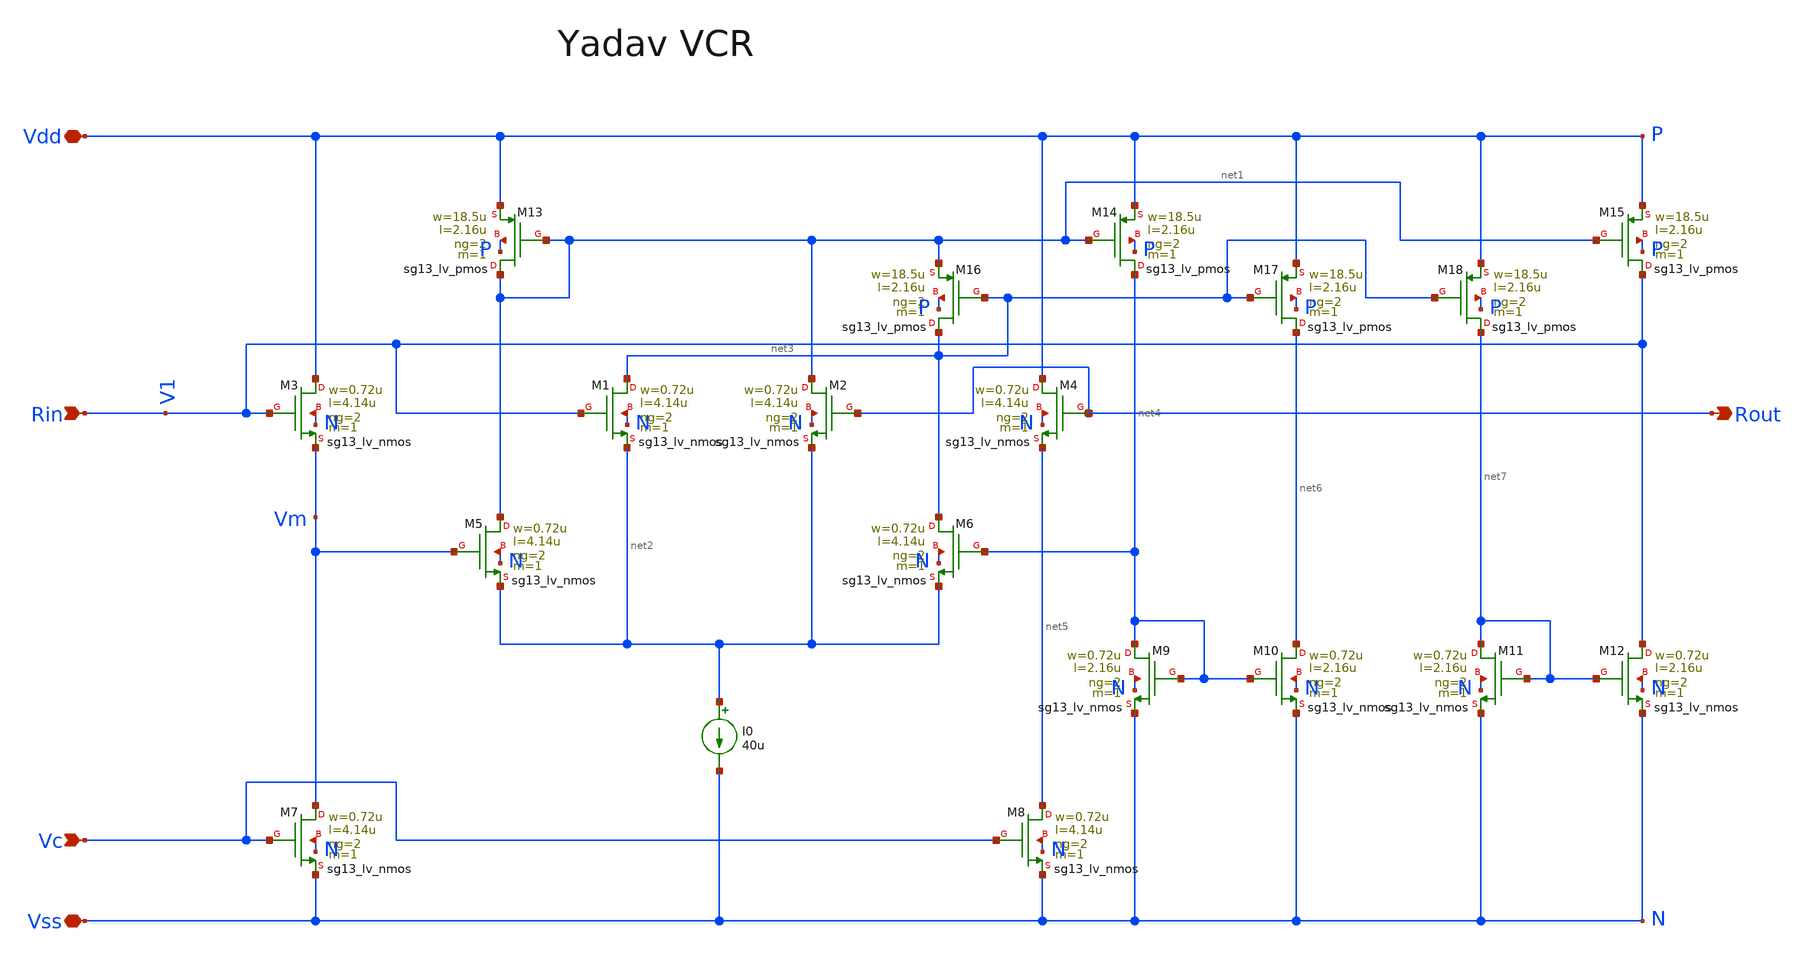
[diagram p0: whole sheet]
** sch_path: macros/heichips26_analog_project/macros/yadav/schematic/xschem/yadav.sch
**.subckt yadav Rin Vc Vss Vdd Rout
*.ipin Rin
*.ipin Vc
*.iopin Vss
*.iopin Vdd
*.opin Rout
XM3 Vdd Rin Vm N sg13_lv_nmos w=0.72u l=4.14u ng=2 m=1 mm_ok=1
XM13 net1 net1 Vdd P sg13_lv_pmos w=18.5u l=2.16u ng=2 m=1 mm_ok=1
XM1 net3 Rin net2 N sg13_lv_nmos w=0.72u l=4.14u ng=2 m=1 mm_ok=1
XM5 net1 Vm net2 N sg13_lv_nmos w=0.72u l=4.14u ng=2 m=1 mm_ok=1
XM2 net1 Rout net2 N sg13_lv_nmos w=0.72u l=4.14u ng=2 m=1 mm_ok=1
XM16 net3 net3 net1 P sg13_lv_pmos w=18.5u l=2.16u ng=2 m=1 mm_ok=1
XM7 Vm Vc Vss N sg13_lv_nmos w=0.72u l=4.14u ng=2 m=1 mm_ok=1
XM6 net3 net4 net2 N sg13_lv_nmos w=0.72u l=4.14u ng=2 m=1 mm_ok=1
XM14 net4 net1 Vdd P sg13_lv_pmos w=18.5u l=2.16u ng=2 m=1 mm_ok=1
XM8 net5 Vc Vss N sg13_lv_nmos w=0.72u l=4.14u ng=2 m=1 mm_ok=1
XM4 Vdd Rout net5 N sg13_lv_nmos w=0.72u l=4.14u ng=2 m=1 mm_ok=1
XM9 net4 net4 Vss N sg13_lv_nmos w=0.72u l=2.16u ng=2 m=1 mm_ok=1
XM10 net6 net4 Vss N sg13_lv_nmos w=0.72u l=2.16u ng=2 m=1 mm_ok=1
XM17 net6 net3 Vdd P sg13_lv_pmos w=18.5u l=2.16u ng=2 m=1 mm_ok=1
XM18 net7 net3 Vdd P sg13_lv_pmos w=18.5u l=2.16u ng=2 m=1 mm_ok=1
XM11 net7 net7 Vss N sg13_lv_nmos w=0.72u l=2.16u ng=2 m=1 mm_ok=1
XM12 Rin net7 Vss N sg13_lv_nmos w=0.72u l=2.16u ng=2 m=1 mm_ok=1
XM15 Rin net1 Vdd P sg13_lv_pmos w=18.5u l=2.16u ng=2 m=1 mm_ok=1
I0 net2 Vss 40u
**.ends
.end
